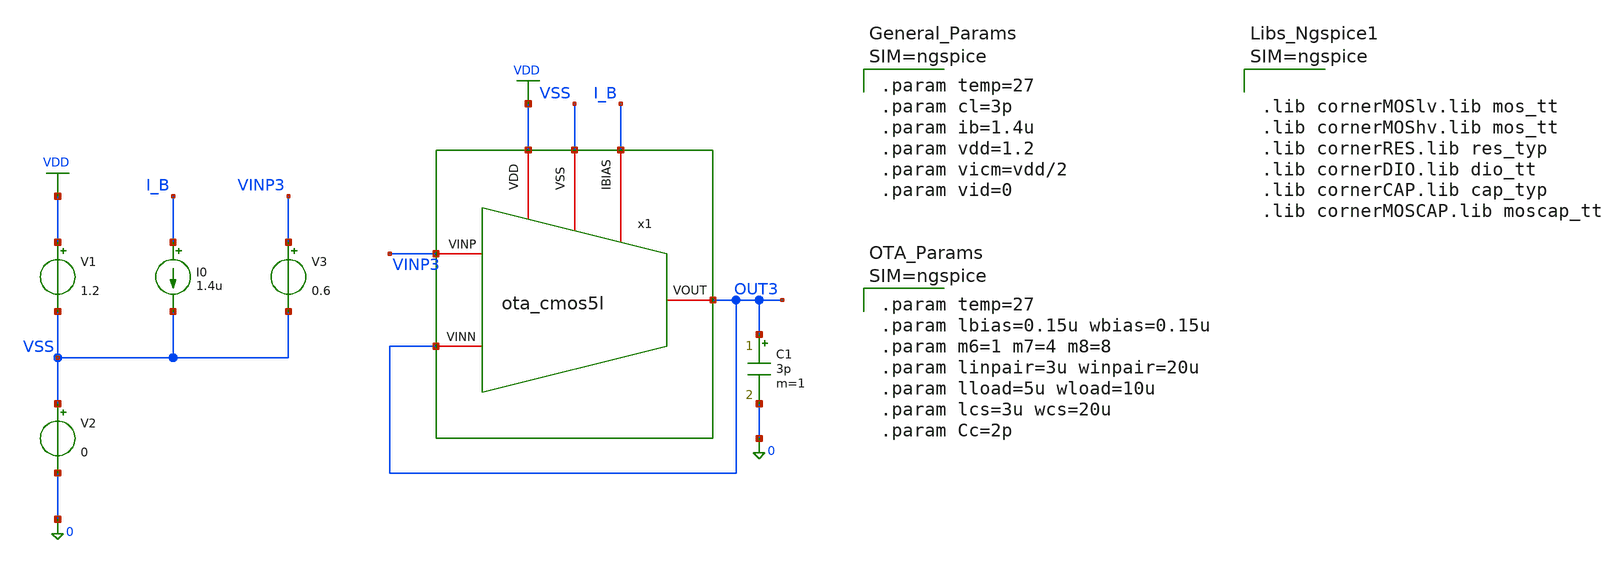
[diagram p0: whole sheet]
** sch_path: xschem/ota_cmos5l/tb/tb_ota_cmos5l_icmr/tb_ota_cmos5l_icmr.sch
**.subckt tb_ota_cmos5l_icmr
x1 VSS I_B VDD OUT3 VINP3 OUT3 ota_cmos5l
C1 OUT3 0 3p m=1
I0 I_B VSS 1.4u
V1 VDD VSS 1.2
V2 VSS 0 0
V3 VINP3 VSS 0.6
**** begin user architecture code



.lib cornerMOSlv.lib mos_tt
.lib cornerMOShv.lib mos_tt
.lib cornerRES.lib res_typ
.lib cornerDIO.lib dio_tt
.lib cornerCAP.lib cap_typ
.lib cornerMOSCAP.lib moscap_tt





.param temp=27
.param cl=3p
.param ib=1.4u
.param vdd=1.2
.param vicm=vdd/2
.param vid=0





.param temp=27
.param lbias=0.15u wbias=0.15u
.param m6=1 m7=4 m8=8
.param linpair=3u winpair=20u
.param lload=5u wload=10u
.param lcs=3u wcs=20u
.param Cc=2p





.control
destroy all
save all
shell mkdir -p result

alter @v3[acmag] = 0

dc v3 0 1.2 2m

let v_in  = v(vinp3)
let v_out = v(out3)

let track_error_mv = abs(v_out - v_in) * 1000

let buffer_gain = deriv(v_out)

* Extract linear ICMR boundary points
* Threshold set at buffer gain > 0.98 (2% gain error margin)
meas dc icmr_min when buffer_gain=0.98 rise=1
meas dc icmr_max when buffer_gain=0.98 fall=1
let icmr_span = icmr_max - icmr_min

write ./result/tb_cg_ota_icmr.raw v_in v_out buffer_gain track_error_mv

* Print summary report to ngspice terminal console
echo "======================================================="
echo "       INPUT COMMON-MODE RANGE (ICMR) RESULTS          "
echo "======================================================="
echo "  Lower ICMR Bound (Vmin, Gain > 0.98) : " $&icmr_min " V"
echo "  Upper ICMR Bound (Vmax, Gain > 0.98) : " $&icmr_max " V"
echo "  Total Linear ICMR Span               : " $&icmr_span " V"
echo "======================================================="

* Display transfer characteristics and tracking performance curves
plot v_out vs v_in
plot buffer_gain vs v_in
plot track_error_mv vs v_in

.endc


**** end user architecture code
**.ends

* expanding   symbol:  /foss/designs/sg13cmos5l_spma_ip__instramp/xschem/ota_cmos5l/ota_cmos5l.sym #
*+ of pins=6
** sym_path: xschem/output_buffer/ota_cmos5l.sym
** sch_path: xschem/output_buffer/ota_cmos5l.sch
.subckt ota_cmos5l VSS IBIAS VDD VINN VINP VOUT
*.iopin IBIAS
*.iopin VDD
*.iopin VSS
*.iopin VOUT
*.iopin VINP
*.iopin VINN
XM6 IBIAS IBIAS VDD VDD sg13_lv_pmos w={wbias} l={lbias} ng=1 m={m6} mm_ok=1
XM7 net1 IBIAS VDD VDD sg13_lv_pmos w={wbias} l={lbias} ng=1 m={m7} mm_ok=1
XM8 VOUT IBIAS VDD VDD sg13_lv_pmos w={wbias} l={lbias} ng=1 m={m8} mm_ok=1
XM1 net2 VINN net1 VDD sg13_lv_pmos w={winpair} l={linpair} ng=1 m=1 mm_ok=1
XM2 net3 VINP net1 VDD sg13_lv_pmos w={winpair} l={linpair} ng=1 m=1 mm_ok=1
XM3 net2 net2 VSS VSS sg13_lv_nmos w={wload} l={lload} ng=1 m=1 mm_ok=1
XM4 net3 net2 VSS VSS sg13_lv_nmos w={wload} l={lload} ng=1 m=1 mm_ok=1
XM5 VOUT net3 VSS VSS sg13_lv_nmos w={wcs} l={lcs} ng=1 m=1 mm_ok=1
XR1 net3 net4 VSS rhigh w=0.5e-6 l=1.95e-6 m=1 b=0 mm_ok=1
.save v(vinp)
.save v(vinn)
.save v(vout)
XC2 VOUT net4 cap_cmomi w=15e-6 l=15e-6 mmin=1 mmax=4 feed=double subblock=0 m=5 mm_ok=1
**** begin user architecture code


.param temp=27
.param lbias=0.15u wbias=0.15u
.param m6=1 m7=4 m8=8
.param linpair=3u winpair=20u
.param lload=5u wload=10u
.param lcs=3u wcs=20u
.param Cc=2p



**** end user architecture code
XC1 VOUT net4 cap_cmomi w=15e-6 l=15e-6 mmin=1 mmax=4 feed=double subblock=0 m=4 mm_ok=1
.ends

.GLOBAL VDD
.end
